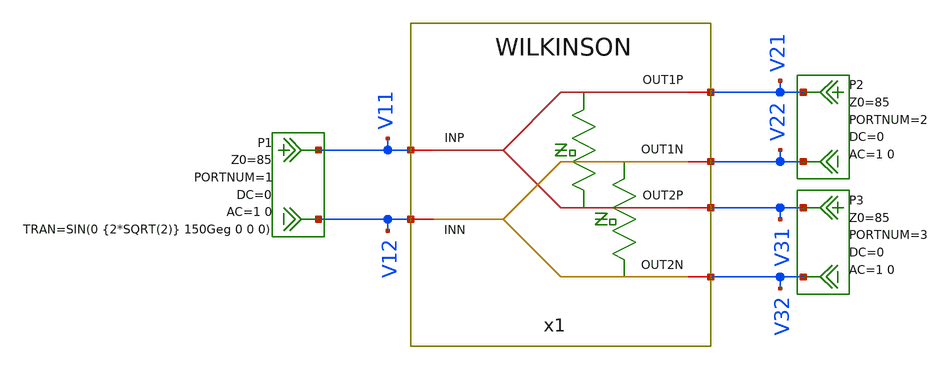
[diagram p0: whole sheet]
** sch_path: mWATTBAT/design_data/xschem/WILKINSON_TB.sch
**.subckt WILKINSON_TB
P1 V11 V12 0 port=1 Z0=85 AC 1 0 SIN(0 {2*SQRT(2)} 150Geg 0 0 0)
P2 V21 V22 0 port=2 Z0=85 AC 1 0
x1 V11 V12 V21 V22 V31 V32 WILKINSON
P3 V31 V32 0 port=3 Z0=85 AC 1 0
**** begin user architecture code


.TRAN 1p 50p 30p
.MEAS TRAN V1 EQN V(V11,V12)
.MEAS TRAN V2 EQN V(V21,V22)
.MEAS TRAN V3 EQN V(V31,V32)
.PRINT TRAN FORMAT=RAW FILE=WILKINSON_TBTRAN.raw V(*) I(*) V1 V2 V3


**** end user architecture code
**.ends

* expanding   symbol:  WILKINSON.sym # of pins=6
** sym_path: mWATTBAT/design_data/xschem/WILKINSON.sym
** sch_path: mWATTBAT/design_data/xschem/WILKINSON.sch
.subckt WILKINSON INP INN OUT1P OUT1N OUT2P OUT2N
*.iopin INP
*.iopin INN
*.iopin OUT1P
*.iopin OUT2N
*.iopin OUT1N
*.iopin OUT2P
ytransline TL17 INP OUT1P ytransline_TL17 len=302.5u lumps=50
.model ytransline_TL17 transline r=13.55k l=331.35n C=91.75p
ytransline TL18 INP OUT2P ytransline_TL18 len=302.5u lumps=50
.model ytransline_TL18 transline r=13.55k l=331.35n C=91.75p
ytransline TL19 INN OUT1N ytransline_TL19 len=302.5u lumps=50
.model ytransline_TL19 transline r=13.55k l=331.35n C=91.75p
ytransline TL20 INN OUT2N ytransline_TL20 len=302.5u lumps=50
.model ytransline_TL20 transline r=13.55k l=331.35n C=91.75p
XR19 OUT1P OUT2P sub! rppd w=3e-6 l=12.51e-6 m=13 b=0 mm_ok=1
XR20 OUT1N OUT2N sub! rppd w=3e-6 l=12.51e-6 m=13 b=0 mm_ok=1
**** begin user architecture code



**** end user architecture code
**** begin user architecture code



.lib $::SG13G2_MODELS/cornerRES.lib res_typ



**** end user architecture code
.ends

.end
